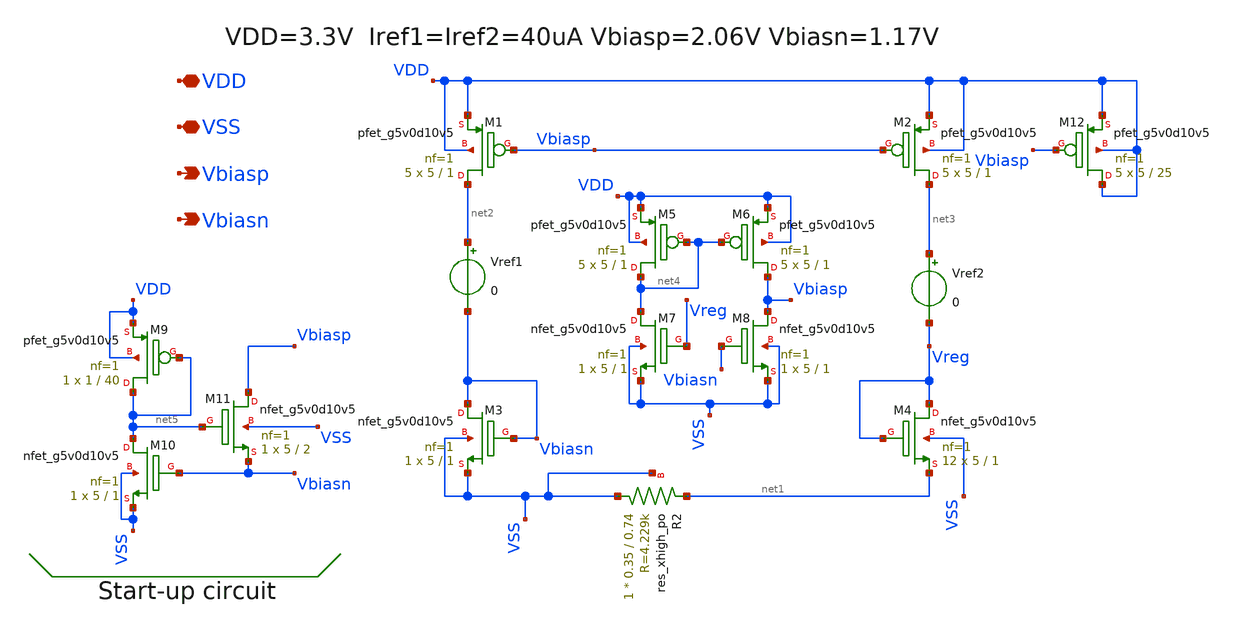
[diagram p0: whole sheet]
** sch_path: xschem/24_beta_multiplier.sch
**.subckt 24_beta_multiplier VDD Vbiasp Vbiasn VSS
*.iopin VDD
*.opin Vbiasp
*.opin Vbiasn
*.iopin VSS
XM1 net2 Vbiasp VDD VDD sky130_fd_pr__pfet_g5v0d10v5 L=1 W=5 nf=1 ad='int((nf+1)/2) * W/nf * 0.29' as='int((nf+2)/2) * W/nf * 0.29'
+ pd='2*int((nf+1)/2) * (W/nf + 0.29)' ps='2*int((nf+2)/2) * (W/nf + 0.29)' nrd='0.29 / W' nrs='0.29 / W'
+ sa=0 sb=0 sd=0 mult=5 m=5
XM3 Vbiasn Vbiasn VSS VSS sky130_fd_pr__nfet_g5v0d10v5 L=1 W=5 nf=1 ad='int((nf+1)/2) * W/nf * 0.29'
+ as='int((nf+2)/2) * W/nf * 0.29' pd='2*int((nf+1)/2) * (W/nf + 0.29)' ps='2*int((nf+2)/2) * (W/nf + 0.29)'
+ nrd='0.29 / W' nrs='0.29 / W' sa=0 sb=0 sd=0 mult=1 m=1
XM2 net3 Vbiasp VDD VDD sky130_fd_pr__pfet_g5v0d10v5 L=1 W=5 nf=1 ad='int((nf+1)/2) * W/nf * 0.29' as='int((nf+2)/2) * W/nf * 0.29'
+ pd='2*int((nf+1)/2) * (W/nf + 0.29)' ps='2*int((nf+2)/2) * (W/nf + 0.29)' nrd='0.29 / W' nrs='0.29 / W'
+ sa=0 sb=0 sd=0 mult=5 m=5
XM4 Vreg Vreg net1 VSS sky130_fd_pr__nfet_g5v0d10v5 L=1 W=5 nf=1 ad='int((nf+1)/2) * W/nf * 0.29' as='int((nf+2)/2) * W/nf * 0.29'
+ pd='2*int((nf+1)/2) * (W/nf + 0.29)' ps='2*int((nf+2)/2) * (W/nf + 0.29)' nrd='0.29 / W' nrs='0.29 / W'
+ sa=0 sb=0 sd=0 mult=12 m=12
Vref1 net2 Vbiasn 0
Vref2 net3 Vreg 0
XR2 VSS net1 VSS sky130_fd_pr__res_xhigh_po W=0.35 L=0.74 mult=1 m=1
XM5 net4 net4 VDD VDD sky130_fd_pr__pfet_g5v0d10v5 L=1 W=5 nf=1 ad='int((nf+1)/2) * W/nf * 0.29' as='int((nf+2)/2) * W/nf * 0.29'
+ pd='2*int((nf+1)/2) * (W/nf + 0.29)' ps='2*int((nf+2)/2) * (W/nf + 0.29)' nrd='0.29 / W' nrs='0.29 / W'
+ sa=0 sb=0 sd=0 mult=5 m=5
XM6 Vbiasp net4 VDD VDD sky130_fd_pr__pfet_g5v0d10v5 L=1 W=5 nf=1 ad='int((nf+1)/2) * W/nf * 0.29' as='int((nf+2)/2) * W/nf * 0.29'
+ pd='2*int((nf+1)/2) * (W/nf + 0.29)' ps='2*int((nf+2)/2) * (W/nf + 0.29)' nrd='0.29 / W' nrs='0.29 / W'
+ sa=0 sb=0 sd=0 mult=5 m=5
XM7 net4 Vreg VSS VSS sky130_fd_pr__nfet_g5v0d10v5 L=1 W=5 nf=1 ad='int((nf+1)/2) * W/nf * 0.29' as='int((nf+2)/2) * W/nf * 0.29'
+ pd='2*int((nf+1)/2) * (W/nf + 0.29)' ps='2*int((nf+2)/2) * (W/nf + 0.29)' nrd='0.29 / W' nrs='0.29 / W'
+ sa=0 sb=0 sd=0 mult=1 m=1
XM8 Vbiasp Vbiasn VSS VSS sky130_fd_pr__nfet_g5v0d10v5 L=1 W=5 nf=1 ad='int((nf+1)/2) * W/nf * 0.29'
+ as='int((nf+2)/2) * W/nf * 0.29' pd='2*int((nf+1)/2) * (W/nf + 0.29)' ps='2*int((nf+2)/2) * (W/nf + 0.29)'
+ nrd='0.29 / W' nrs='0.29 / W' sa=0 sb=0 sd=0 mult=1 m=1
XM9 net5 net5 VDD VDD sky130_fd_pr__pfet_g5v0d10v5 L=40 W=1 nf=1 ad='int((nf+1)/2) * W/nf * 0.29' as='int((nf+2)/2) * W/nf * 0.29'
+ pd='2*int((nf+1)/2) * (W/nf + 0.29)' ps='2*int((nf+2)/2) * (W/nf + 0.29)' nrd='0.29 / W' nrs='0.29 / W'
+ sa=0 sb=0 sd=0 mult=1 m=1
XM10 net5 Vbiasn VSS VSS sky130_fd_pr__nfet_g5v0d10v5 L=1 W=5 nf=1 ad='int((nf+1)/2) * W/nf * 0.29' as='int((nf+2)/2) * W/nf * 0.29'
+ pd='2*int((nf+1)/2) * (W/nf + 0.29)' ps='2*int((nf+2)/2) * (W/nf + 0.29)' nrd='0.29 / W' nrs='0.29 / W'
+ sa=0 sb=0 sd=0 mult=1 m=1
XM11 Vbiasp net5 Vbiasn VSS sky130_fd_pr__nfet_g5v0d10v5 L=2 W=5 nf=1 ad='int((nf+1)/2) * W/nf * 0.29'
+ as='int((nf+2)/2) * W/nf * 0.29' pd='2*int((nf+1)/2) * (W/nf + 0.29)' ps='2*int((nf+2)/2) * (W/nf + 0.29)'
+ nrd='0.29 / W' nrs='0.29 / W' sa=0 sb=0 sd=0 mult=1 m=1
XM12 VDD Vbiasp VDD VDD sky130_fd_pr__pfet_g5v0d10v5 L=25 W=5 nf=1 ad='int((nf+1)/2) * W/nf * 0.29' as='int((nf+2)/2) * W/nf * 0.29'
+ pd='2*int((nf+1)/2) * (W/nf + 0.29)' ps='2*int((nf+2)/2) * (W/nf + 0.29)' nrd='0.29 / W' nrs='0.29 / W'
+ sa=0 sb=0 sd=0 mult=5 m=5
**.ends
.end
